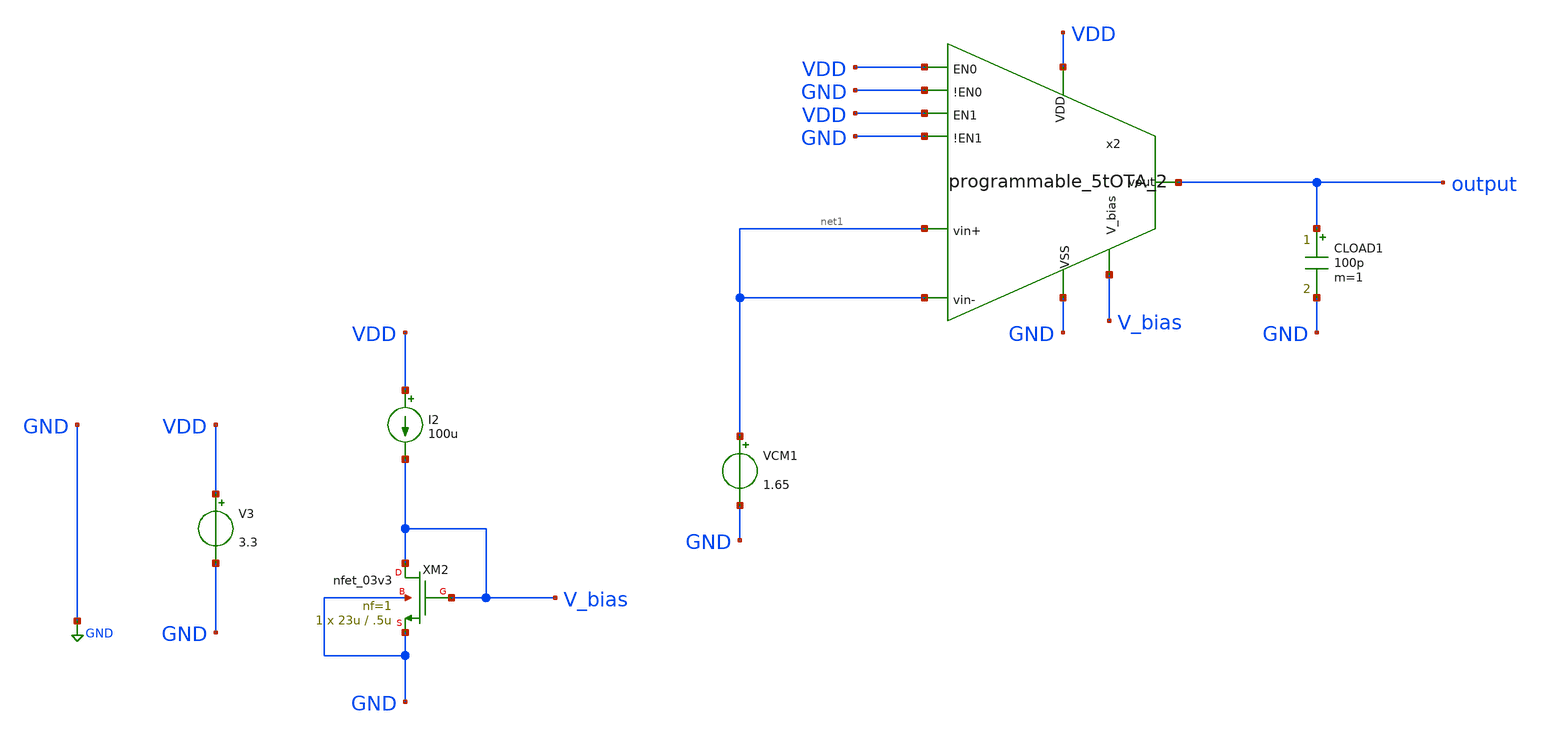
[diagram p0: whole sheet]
** sch_path: designs/libs/core_amps/ota_5t/programmable_5tOTA_op_vdsat_tb2.sch
**.subckt programmable_5tOTA_op_vdsat_tb2
XM2 V_bias V_bias GND GND nfet_03v3 L=.5u W=23u nf=1 ad='int((nf+1)/2) * W/nf * 0.18u' as='int((nf+2)/2) * W/nf * 0.18u'
+ pd='2*int((nf+1)/2) * (W/nf + 0.18u)' ps='2*int((nf+2)/2) * (W/nf + 0.18u)' nrd='0.18u / W' nrs='0.18u / W'
+ sa=0 sb=0 sd=0 m=1
I2 VDD V_bias 100u
V3 VDD GND 3.3
CLOAD1 output GND 100p m=1
x2 VDD VDD GND output VDD GND net1 net1 net2 GND programmable_5tOTA_2
VCM1 net1 GND 1.65
**** begin user architecture code

.include $::180MCU_MODELS/design.ngspice
.lib $::180MCU_MODELS/sm141064.ngspice typical



.control
op

show all

.endc



**** end user architecture code
**.ends
.GLOBAL GND
.end
